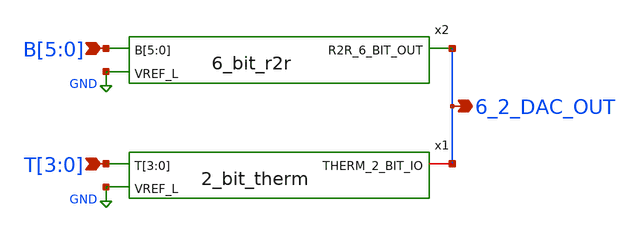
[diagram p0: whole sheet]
** sch_path: xschem/6_2_dac.sch
**.subckt 6_2_dac B[5],B[4],B[3],B[2],B[1],B[0] T[3],T[2],T[1],T[0] 6_2_DAC_OUT
*.ipin B[5],B[4],B[3],B[2],B[1],B[0]
*.ipin T[3],T[2],T[1],T[0]
*.opin 6_2_DAC_OUT
x1 6_2_DAC_OUT GND T[3] T[2] T[1] T[0] 2_bit_therm
x2 B[5] B[4] B[3] B[2] B[1] B[0] GND 6_2_DAC_OUT 6_bit_r2r
**.ends
.GLOBAL GND
.end
